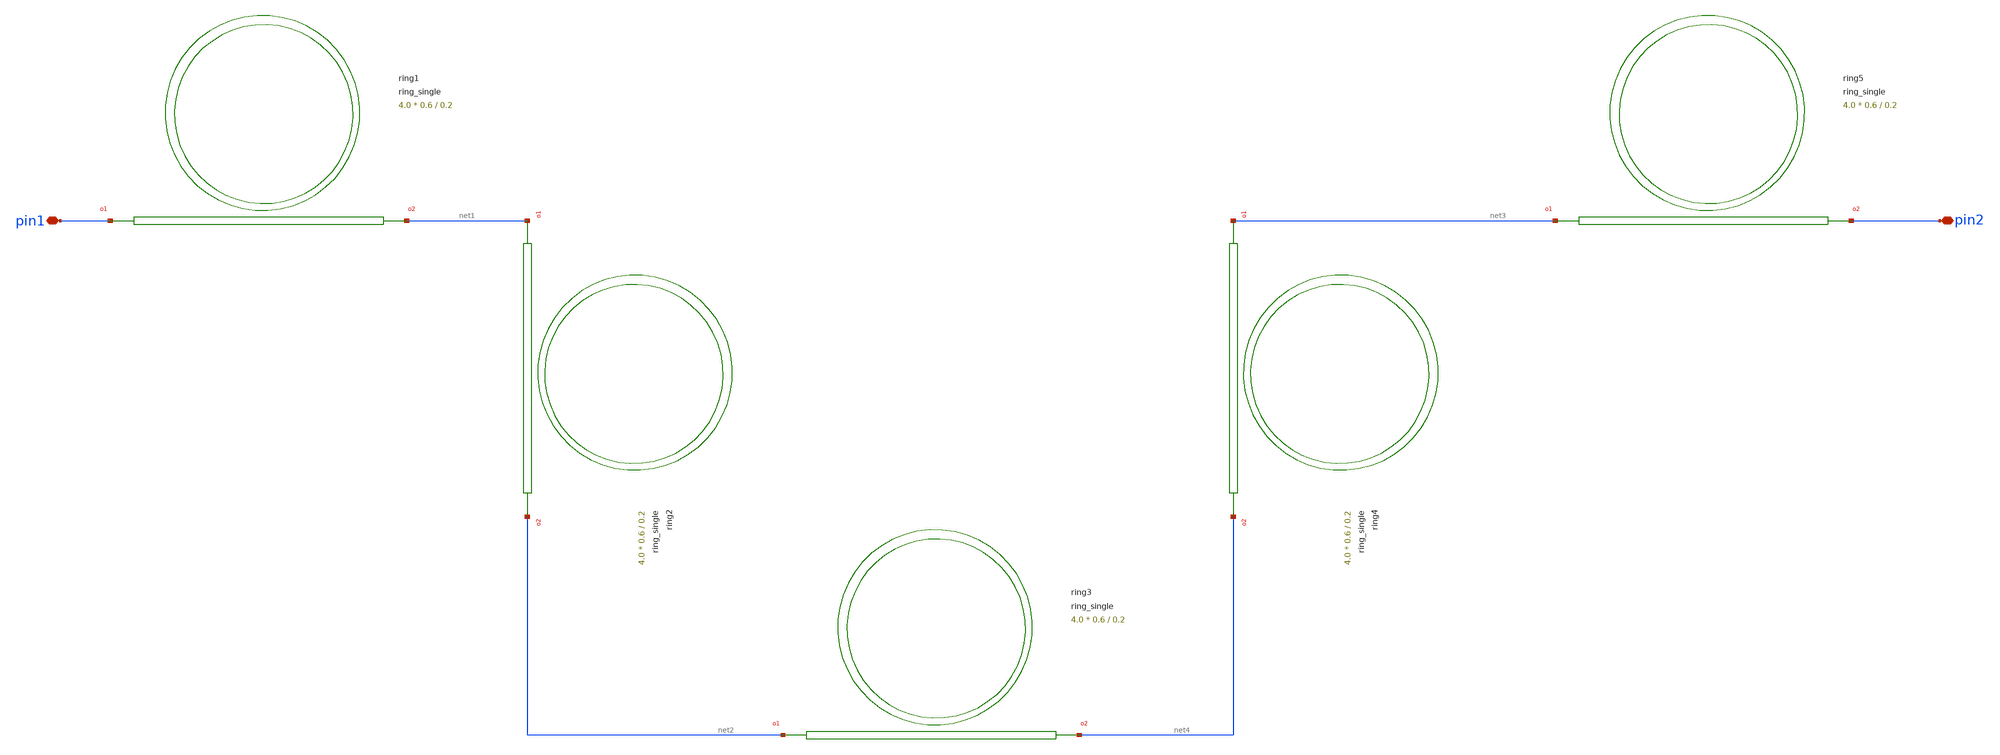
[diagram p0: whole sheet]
** sch_path: cells/xschem/tests/test_ring_single.sch
* SPDX-FileCopyrightText: 2023 Mabrains Company
* Licensed under the GNU GENERAL PUBLIC License, Version 3.0 (the "License");
* you may not use this file except in compliance with the License.
* GNU GENERAL PUBLIC LICENSE
* Version 3, 29 June 2007
* This program is free software: you can redistribute it and/or modify
* it under the terms of the GNU General Public License as published
* by the Free Software Foundation, either 3 of the License, or
* (at your option) any later version.
* This program is distributed in the hope that it will be useful,
* but WITHOUT ANY WARRANTY; without even the implied warranty of
* MERCHANTABILITY or FITNESS FOR A PARTICULAR PURPOSE.  See the
* GNU General Public License for more details.
* You should have received a copy of the GNU General Public License
* along with this program.  If not, see <https://www.gnu.org/licenses/>.
* SPDX-License-Identifier: GPL-3.0
**.subckt test_ring_single pin1 pin2
*.iopin pin1
*.iopin pin2
Pring1 pin1 net1 ring_single gap=0.2 radius=10.0 length_x=4.0 length_y=0.6
Pring2 net1 net2 ring_single gap=0.2 radius=10.0 length_x=4.0 length_y=0.6
Pring3 net2 net4 ring_single gap=0.2 radius=10.0 length_x=4.0 length_y=0.6
Pring4 net3 net4 ring_single gap=0.2 radius=10.0 length_x=4.0 length_y=0.6
Pring5 net3 pin2 ring_single gap=0.2 radius=10.0 length_x=4.0 length_y=0.6
**.ends
.end
